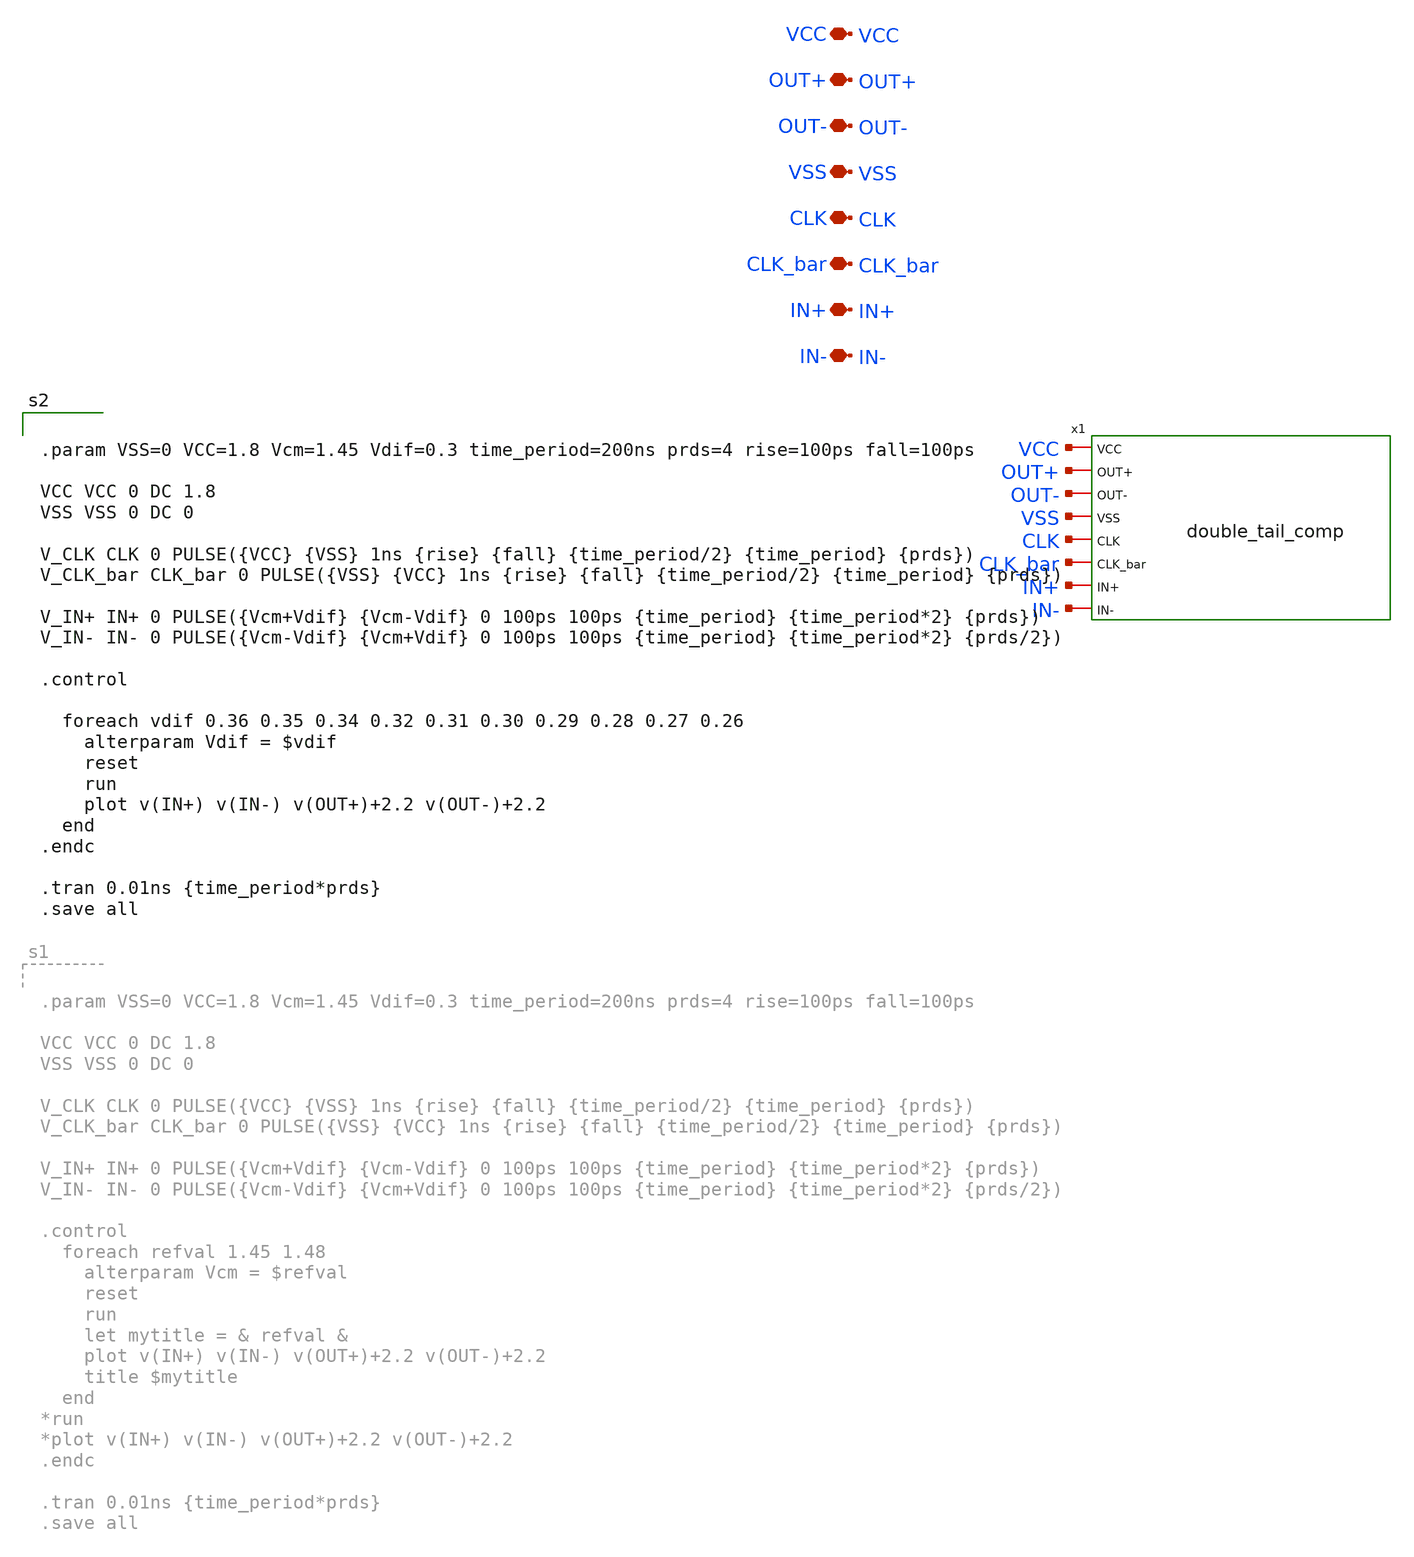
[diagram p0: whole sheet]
** sch_path: voltage_comp/dt_comp_test.sch
**.subckt dt_comp_test OUT- VSS VCC OUT+ IN+ IN- CLK CLK_bar
*.iopin OUT-
*.iopin VSS
*.iopin VCC
*.iopin OUT+
*.iopin IN+
*.iopin IN-
*.iopin CLK
*.iopin CLK_bar
x1 VCC OUT+ OUT- VSS CLK CLK_bar IN+ IN- double_tail_comp
**** begin user architecture code

** opencircuitdesign pdks install
.lib $::SKYWATER_MODELS/sky130.lib.spice tt



.param VSS=0 VCC=1.8 Vcm=1.45 Vdif=0.3 time_period=200ns prds=4 rise=100ps fall=100ps

VCC VCC 0 DC 1.8
VSS VSS 0 DC 0

V_CLK CLK 0 PULSE({VCC} {VSS} 1ns {rise} {fall} {time_period/2} {time_period} {prds})
V_CLK_bar CLK_bar 0 PULSE({VSS} {VCC} 1ns {rise} {fall} {time_period/2} {time_period} {prds})

V_IN+ IN+ 0 PULSE({Vcm+Vdif} {Vcm-Vdif} 0 100ps 100ps {time_period} {time_period*2} {prds})
V_IN- IN- 0 PULSE({Vcm-Vdif} {Vcm+Vdif} 0 100ps 100ps {time_period} {time_period*2} {prds/2})

.control

  foreach vdif 0.36 0.35 0.34 0.32 0.31 0.30 0.29 0.28 0.27 0.26
    alterparam Vdif = $vdif
    reset
    run
    plot v(IN+) v(IN-) v(OUT+)+2.2 v(OUT-)+2.2
  end
.endc

.tran 0.01ns {time_period*prds}
.save all


**** end user architecture code
**.ends

* expanding   symbol:  voltage_comp/double_tail_comp.sym # of pins=8
** sym_path: voltage_comp/double_tail_comp.sym
** sch_path: voltage_comp/double_tail_comp.sch
.subckt double_tail_comp VCC OUT+ OUT- VSS CLK CLK_bar IN+ IN-
*.iopin OUT-
*.iopin VSS
*.iopin VCC
*.iopin OUT+
*.iopin IN+
*.iopin IN-
*.iopin CLK
*.iopin CLK_bar
XM2 OUT- OUT+ VSS VSS sky130_fd_pr__nfet_01v8 L=0.15 W=1 nf=1 ad='int((1 + 1)/2) * 1 / 1 * 0.29' as='int((1 + 2)/2) * 1 / 1 * 0.29'
+ pd='2*int((1 + 1)/2) * (1 / 1 + 0.29)' ps='2*int((1 + 2)/2) * (1 / 1 + 0.29)' nrd='0.29 / 1 ' nrs='0.29 / 1 '
+ sa=0 sb=0 sd=0 mult=1 m=1
XM11 OUT- OUT+ net2 net2 sky130_fd_pr__pfet_01v8 L=0.15 W=1 nf=1 ad='int((nf+1)/2) * W/nf * 0.29' as='int((nf+2)/2) * W/nf * 0.29'
+ pd='2*int((nf+1)/2) * (W/nf + 0.29)' ps='2*int((nf+2)/2) * (W/nf + 0.29)' nrd='0.29 / W' nrs='0.29 / W'
+ sa=0 sb=0 sd=0 mult=1 m=1
XM1 OUT+ OUT- VSS VSS sky130_fd_pr__nfet_01v8 L=0.15 W=1 nf=1 ad='int((1 + 1)/2) * 1 / 1 * 0.29' as='int((1 + 2)/2) * 1 / 1 * 0.29'
+ pd='2*int((1 + 1)/2) * (1 / 1 + 0.29)' ps='2*int((1 + 2)/2) * (1 / 1 + 0.29)' nrd='0.29 / 1 ' nrs='0.29 / 1 '
+ sa=0 sb=0 sd=0 mult=1 m=1
XM3 OUT+ OUT- net2 net2 sky130_fd_pr__pfet_01v8 L=0.15 W=1 nf=1 ad='int((nf+1)/2) * W/nf * 0.29' as='int((nf+2)/2) * W/nf * 0.29'
+ pd='2*int((nf+1)/2) * (W/nf + 0.29)' ps='2*int((nf+2)/2) * (W/nf + 0.29)' nrd='0.29 / W' nrs='0.29 / W'
+ sa=0 sb=0 sd=0 mult=1 m=1
XM4 OUT+ Di- VSS VSS sky130_fd_pr__nfet_01v8 L=0.15 W=1 nf=1 ad='int((1 + 1)/2) * 1 / 1 * 0.29' as='int((1 + 2)/2) * 1 / 1 * 0.29'
+ pd='2*int((1 + 1)/2) * (1 / 1 + 0.29)' ps='2*int((1 + 2)/2) * (1 / 1 + 0.29)' nrd='0.29 / 1 ' nrs='0.29 / 1 '
+ sa=0 sb=0 sd=0 mult=1 m=1
XM5 OUT- Di+ VSS VSS sky130_fd_pr__nfet_01v8 L=0.15 W=1 nf=1 ad='int((1 + 1)/2) * 1 / 1 * 0.29' as='int((1 + 2)/2) * 1 / 1 * 0.29'
+ pd='2*int((1 + 1)/2) * (1 / 1 + 0.29)' ps='2*int((1 + 2)/2) * (1 / 1 + 0.29)' nrd='0.29 / 1 ' nrs='0.29 / 1 '
+ sa=0 sb=0 sd=0 mult=1 m=1
XM6 net2 CLK_bar VCC VCC sky130_fd_pr__pfet_01v8 L=0.15 W=1 nf=1 ad='int((nf+1)/2) * W/nf * 0.29' as='int((nf+2)/2) * W/nf * 0.29'
+ pd='2*int((nf+1)/2) * (W/nf + 0.29)' ps='2*int((nf+2)/2) * (W/nf + 0.29)' nrd='0.29 / W' nrs='0.29 / W'
+ sa=0 sb=0 sd=0 mult=1 m=1
XM8 Di- CLK VCC VCC sky130_fd_pr__pfet_01v8 L=0.15 W=1 nf=1 ad='int((nf+1)/2) * W/nf * 0.29' as='int((nf+2)/2) * W/nf * 0.29'
+ pd='2*int((nf+1)/2) * (W/nf + 0.29)' ps='2*int((nf+2)/2) * (W/nf + 0.29)' nrd='0.29 / W' nrs='0.29 / W'
+ sa=0 sb=0 sd=0 mult=1 m=1
XM9 Di- IN+ net1 net1 sky130_fd_pr__nfet_01v8 L=0.15 W=1 nf=1 ad='int((1 + 1)/2) * 1 / 1 * 0.29' as='int((1 + 2)/2) * 1 / 1 * 0.29'
+ pd='2*int((1 + 1)/2) * (1 / 1 + 0.29)' ps='2*int((1 + 2)/2) * (1 / 1 + 0.29)' nrd='0.29 / 1 ' nrs='0.29 / 1 '
+ sa=0 sb=0 sd=0 mult=1 m=1
XM7 Di+ CLK VCC VCC sky130_fd_pr__pfet_01v8 L=0.15 W=1 nf=1 ad='int((nf+1)/2) * W/nf * 0.29' as='int((nf+2)/2) * W/nf * 0.29'
+ pd='2*int((nf+1)/2) * (W/nf + 0.29)' ps='2*int((nf+2)/2) * (W/nf + 0.29)' nrd='0.29 / W' nrs='0.29 / W'
+ sa=0 sb=0 sd=0 mult=1 m=1
XM10 Di+ IN- net1 net1 sky130_fd_pr__nfet_01v8 L=0.15 W=1 nf=1 ad='int((1 + 1)/2) * 1 / 1 * 0.29' as='int((1 + 2)/2) * 1 / 1 * 0.29'
+ pd='2*int((1 + 1)/2) * (1 / 1 + 0.29)' ps='2*int((1 + 2)/2) * (1 / 1 + 0.29)' nrd='0.29 / 1 ' nrs='0.29 / 1 '
+ sa=0 sb=0 sd=0 mult=1 m=1
XM12 net1 CLK VSS VSS sky130_fd_pr__nfet_01v8 L=0.15 W=1 nf=1 ad='int((1 + 1)/2) * 1 / 1 * 0.29' as='int((1 + 2)/2) * 1 / 1 * 0.29'
+ pd='2*int((1 + 1)/2) * (1 / 1 + 0.29)' ps='2*int((1 + 2)/2) * (1 / 1 + 0.29)' nrd='0.29 / 1 ' nrs='0.29 / 1 '
+ sa=0 sb=0 sd=0 mult=1 m=1
XR2 VSS net1 VSS sky130_fd_pr__res_high_po W=1 L=1 mult=1 m=1
.ends

.end
